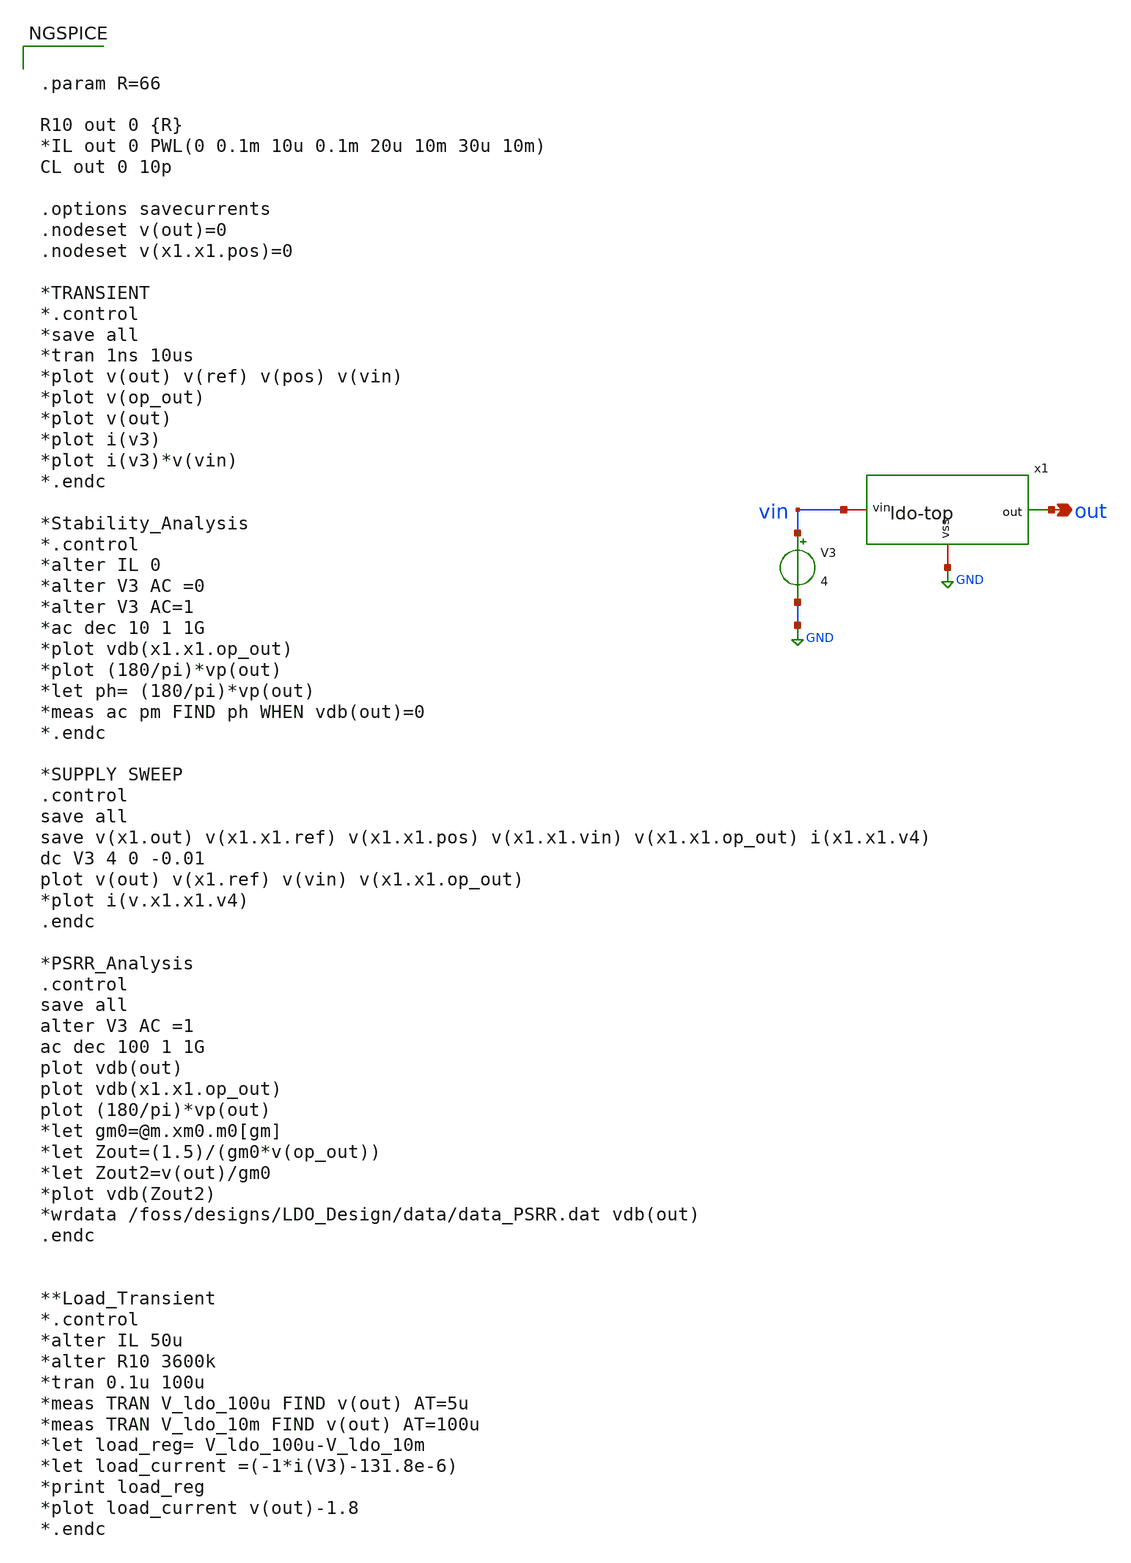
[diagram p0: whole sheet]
** sch_path: LDO/xschem/ldo-top/test/ldo-top-test.sch

.include $env(PDK_ROOT)/$env(PDK)/libs.tech/ngspice/design.ngspice

.lib $env(PDK_ROOT)/$env(PDK)/libs.tech/ngspice/sm141064.ngspice typical
.lib $env(PDK_ROOT)/$env(PDK)/libs.tech/ngspice/sm141064.ngspice mimcap_statistical
.lib $env(PDK_ROOT)/$env(PDK)/libs.tech/ngspice/sm141064.ngspice cap_mim
.lib $env(PDK_ROOT)/$env(PDK)/libs.tech/ngspice/sm141064.ngspice res_typical
.lib $env(PDK_ROOT)/$env(PDK)/libs.tech/ngspice/sm141064.ngspice bjt_typical
.lib $env(PDK_ROOT)/$env(PDK)/libs.tech/ngspice/sm141064.ngspice moscap_typical


**.subckt ldo-top-test out
*.opin out
V3 vin GND 4
x1 vin out GND ldo-top
**** begin user architecture code

.param R=66

R10 out 0 {R}
*IL out 0 PWL(0 0.1m 10u 0.1m 20u 10m 30u 10m)
CL out 0 10p

.options savecurrents
.nodeset v(out)=0
.nodeset v(x1.x1.pos)=0

*TRANSIENT
*.control
*save all
*tran 1ns 10us
*plot v(out) v(ref) v(pos) v(vin)
*plot v(op_out)
*plot v(out)
*plot i(v3)
*plot i(v3)*v(vin)
*.endc

*Stability_Analysis
*.control
*alter IL 0
*alter V3 AC =0
*alter V3 AC=1
*ac dec 10 1 1G
*plot vdb(x1.x1.op_out)
*plot (180/pi)*vp(out)
*let ph= (180/pi)*vp(out)
*meas ac pm FIND ph WHEN vdb(out)=0
*.endc

*SUPPLY SWEEP
.control
save all
save v(x1.out) v(x1.x1.ref) v(x1.x1.pos) v(x1.x1.vin) v(x1.x1.op_out) i(x1.x1.v4)
dc V3 4 0 -0.01
plot v(out) v(x1.ref) v(vin) v(x1.x1.op_out)
*plot i(v.x1.x1.v4)
.endc

*PSRR_Analysis
.control
save all
alter V3 AC =1
ac dec 100 1 1G
plot vdb(out)
plot vdb(x1.x1.op_out)
plot (180/pi)*vp(out)
*let gm0=@m.xm0.m0[gm]
*let Zout=(1.5)/(gm0*v(op_out))
*let Zout2=v(out)/gm0
*plot vdb(Zout2)
*wrdata /foss/designs/LDO_Design/data/data_PSRR.dat vdb(out)
.endc


**Load_Transient
*.control
*alter IL 50u
*alter R10 3600k
*tran 0.1u 100u
*meas TRAN V_ldo_100u FIND v(out) AT=5u
*meas TRAN V_ldo_10m FIND v(out) AT=100u
*let load_reg= V_ldo_100u-V_ldo_10m
*let load_current =(-1*i(V3)-131.8e-6)
*print load_reg
*plot load_current v(out)-1.8
*.endc

**** end user architecture code
**.ends
.GLOBAL GND
.end
